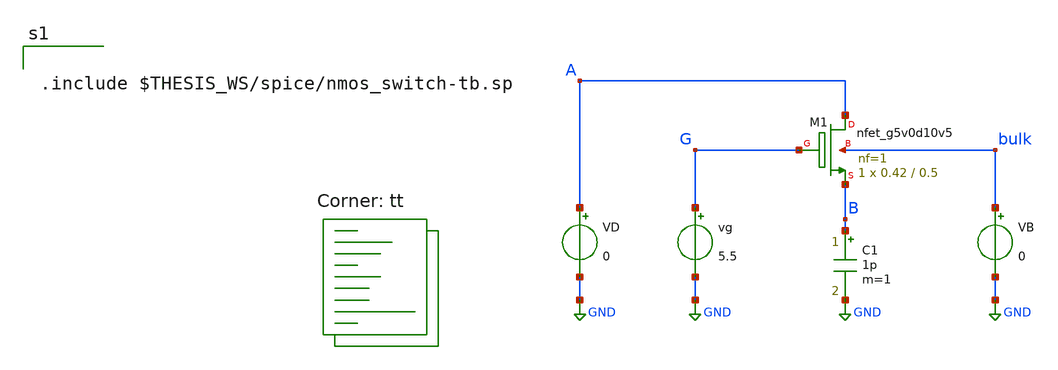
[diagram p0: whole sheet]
** sch_path: xschem/nmos_switch-tb.sch
**.subckt nmos_switch-tb
vg G GND 5.5
XM1 A G B bulk sky130_fd_pr__nfet_g5v0d10v5 L=0.5 W=0.42 nf=1 ad='int((nf+1)/2) * W/nf * 0.29' as='int((nf+2)/2) * W/nf * 0.29'
+ pd='2*int((nf+1)/2) * (W/nf + 0.29)' ps='2*int((nf+2)/2) * (W/nf + 0.29)' nrd='0.29 / W' nrs='0.29 / W'
+ sa=0 sb=0 sd=0 mult=1 m=1
C1 B GND 1p m=1
VD A GND 0
VB bulk GND 0
**** begin user architecture code
.lib $::SKYWATER_MODELS/sky130.lib.spice tt


.include $THESIS_WS/spice/nmos_switch-tb.sp

**** end user architecture code
**.ends
.GLOBAL GND
.end
